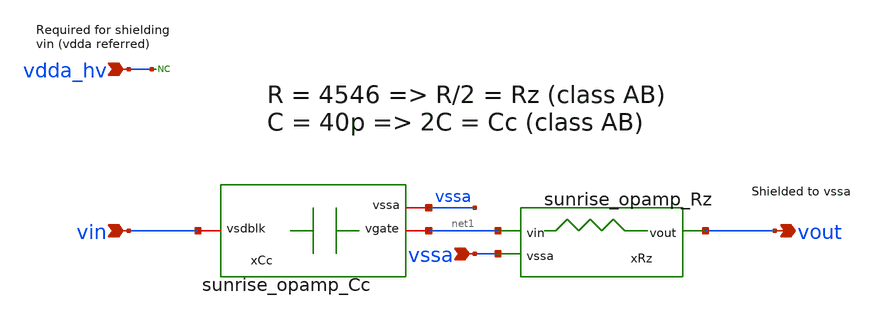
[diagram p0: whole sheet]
** sch_path: Schematics_Layout/sunrise_opamp_pcomp/sunrise_opamp_pcomp.sch
**.subckt sunrise_opamp_pcomp vssa vout vin vdda_hv
*.ipin vssa
*.opin vout
*.ipin vin
*.ipin vdda_hv
xCc net1 vin vssa sunrise_opamp_Cc
xRz vssa vout net1 sunrise_opamp_Rz
* noconn vdda_hv
**.ends
.end
